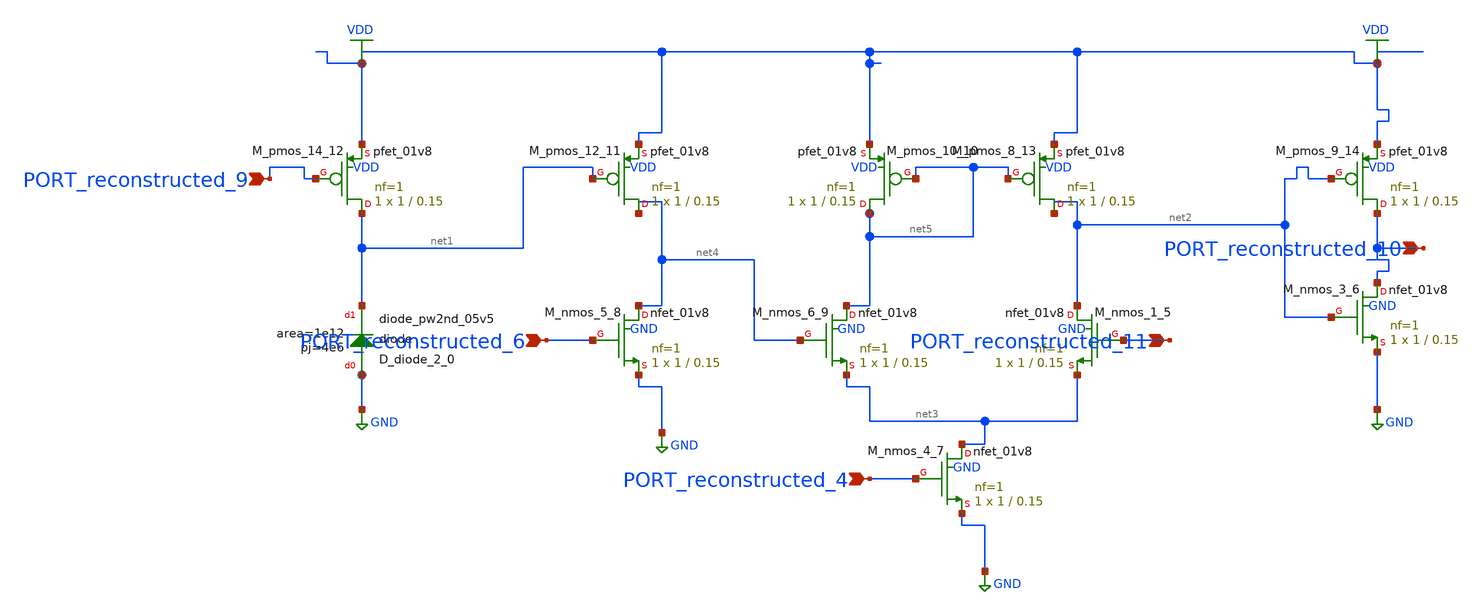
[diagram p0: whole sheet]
** sch_path: schematics/no_doi_108_001_crop1.sch
**.subckt no_doi_108_001_crop1 PORT_reconstructed_6 PORT_reconstructed_11 PORT_reconstructed_4
*+ PORT_reconstructed_9 PORT_reconstructed_10
*.ipin PORT_reconstructed_6
*.ipin PORT_reconstructed_11
*.ipin PORT_reconstructed_4
*.ipin PORT_reconstructed_9
*.ipin PORT_reconstructed_10
XD_diode_2_0 GND net1 sky130_fd_pr__diode_pw2nd_05v5 area=1e12 pj=4e6
XM_nmos_1_5 net2 PORT_reconstructed_11 net3 GND sky130_fd_pr__nfet_01v8 L=0.15 W=1 nf=1 ad='int((1 + 1)/2) * 1 / 1 * 0.29'
+ as='int((1 + 2)/2) * 1 / 1 * 0.29' pd='2*int((1 + 1)/2) * (1 / 1 + 0.29)' ps='2*int((1 + 2)/2) * (1 / 1 + 0.29)'
+ nrd='0.29 / 1 ' nrs='0.29 / 1 ' sa=0 sb=0 sd=0 mult=1 m=1
XM_nmos_3_6 PORT_reconstructed_10 net2 GND GND sky130_fd_pr__nfet_01v8 L=0.15 W=1 nf=1 ad='int((1 + 1)/2) * 1 / 1 * 0.29'
+ as='int((1 + 2)/2) * 1 / 1 * 0.29' pd='2*int((1 + 1)/2) * (1 / 1 + 0.29)' ps='2*int((1 + 2)/2) * (1 / 1 + 0.29)'
+ nrd='0.29 / 1 ' nrs='0.29 / 1 ' sa=0 sb=0 sd=0 mult=1 m=1
XM_nmos_4_7 net3 PORT_reconstructed_4 GND GND sky130_fd_pr__nfet_01v8 L=0.15 W=1 nf=1 ad='int((1 + 1)/2) * 1 / 1 * 0.29'
+ as='int((1 + 2)/2) * 1 / 1 * 0.29' pd='2*int((1 + 1)/2) * (1 / 1 + 0.29)' ps='2*int((1 + 2)/2) * (1 / 1 + 0.29)'
+ nrd='0.29 / 1 ' nrs='0.29 / 1 ' sa=0 sb=0 sd=0 mult=1 m=1
XM_nmos_5_8 net4 PORT_reconstructed_6 GND GND sky130_fd_pr__nfet_01v8 L=0.15 W=1 nf=1 ad='int((1 + 1)/2) * 1 / 1 * 0.29'
+ as='int((1 + 2)/2) * 1 / 1 * 0.29' pd='2*int((1 + 1)/2) * (1 / 1 + 0.29)' ps='2*int((1 + 2)/2) * (1 / 1 + 0.29)'
+ nrd='0.29 / 1 ' nrs='0.29 / 1 ' sa=0 sb=0 sd=0 mult=1 m=1
XM_nmos_6_9 net5 net4 net3 GND sky130_fd_pr__nfet_01v8 L=0.15 W=1 nf=1 ad='int((1 + 1)/2) * 1 / 1 * 0.29'
+ as='int((1 + 2)/2) * 1 / 1 * 0.29' pd='2*int((1 + 1)/2) * (1 / 1 + 0.29)' ps='2*int((1 + 2)/2) * (1 / 1 + 0.29)'
+ nrd='0.29 / 1 ' nrs='0.29 / 1 ' sa=0 sb=0 sd=0 mult=1 m=1
XM_pmos_10_10 net5 net5 VDD VDD sky130_fd_pr__pfet_01v8 L=0.15 W=1 nf=1 ad='int((1 + 1)/2) * 1 / 1 * 0.29'
+ as='int((1 + 2)/2) * 1 / 1 * 0.29' pd='2*int((1 + 1)/2) * (1 / 1 + 0.29)' ps='2*int((1 + 2)/2) * (1 / 1 + 0.29)'
+ nrd='0.29 / 1 ' nrs='0.29 / 1 ' sa=0 sb=0 sd=0 mult=1 m=1
XM_pmos_12_11 net4 net1 VDD VDD sky130_fd_pr__pfet_01v8 L=0.15 W=1 nf=1 ad='int((1 + 1)/2) * 1 / 1 * 0.29'
+ as='int((1 + 2)/2) * 1 / 1 * 0.29' pd='2*int((1 + 1)/2) * (1 / 1 + 0.29)' ps='2*int((1 + 2)/2) * (1 / 1 + 0.29)'
+ nrd='0.29 / 1 ' nrs='0.29 / 1 ' sa=0 sb=0 sd=0 mult=1 m=1
XM_pmos_14_12 net1 PORT_reconstructed_9 VDD VDD sky130_fd_pr__pfet_01v8 L=0.15 W=1 nf=1 ad='int((1 + 1)/2) * 1 / 1 * 0.29'
+ as='int((1 + 2)/2) * 1 / 1 * 0.29' pd='2*int((1 + 1)/2) * (1 / 1 + 0.29)' ps='2*int((1 + 2)/2) * (1 / 1 + 0.29)'
+ nrd='0.29 / 1 ' nrs='0.29 / 1 ' sa=0 sb=0 sd=0 mult=1 m=1
XM_pmos_8_13 net2 net5 VDD VDD sky130_fd_pr__pfet_01v8 L=0.15 W=1 nf=1 ad='int((1 + 1)/2) * 1 / 1 * 0.29'
+ as='int((1 + 2)/2) * 1 / 1 * 0.29' pd='2*int((1 + 1)/2) * (1 / 1 + 0.29)' ps='2*int((1 + 2)/2) * (1 / 1 + 0.29)'
+ nrd='0.29 / 1 ' nrs='0.29 / 1 ' sa=0 sb=0 sd=0 mult=1 m=1
XM_pmos_9_14 PORT_reconstructed_10 net2 VDD VDD sky130_fd_pr__pfet_01v8 L=0.15 W=1 nf=1 ad='int((1 + 1)/2) * 1 / 1 * 0.29'
+ as='int((1 + 2)/2) * 1 / 1 * 0.29' pd='2*int((1 + 1)/2) * (1 / 1 + 0.29)' ps='2*int((1 + 2)/2) * (1 / 1 + 0.29)'
+ nrd='0.29 / 1 ' nrs='0.29 / 1 ' sa=0 sb=0 sd=0 mult=1 m=1
**.ends
.GLOBAL GND
.GLOBAL VDD
.end
